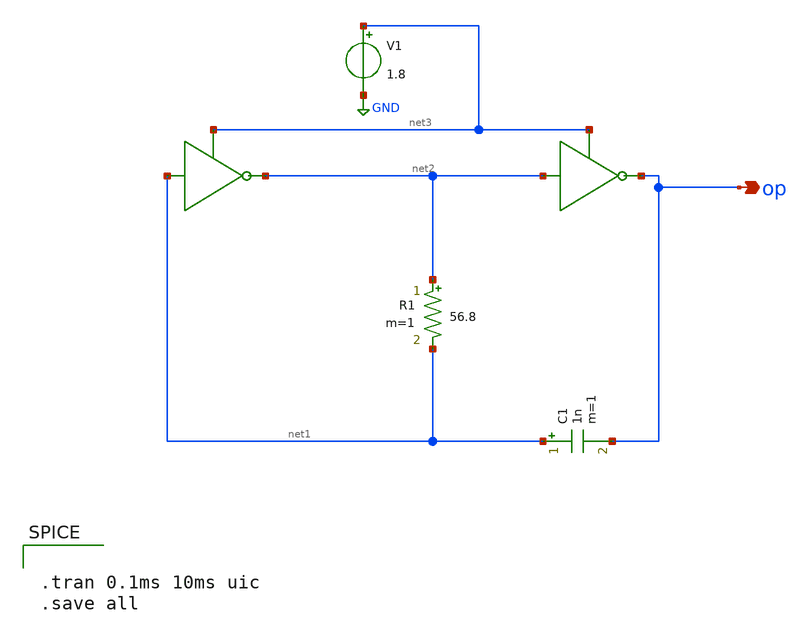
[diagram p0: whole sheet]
** sch_path: Current Sensor/sq_wave.sch
**.subckt sq_wave op
*.opin op
C1 net1 op 1n m=1
R1 net2 net1 56.8 m=1
V1 net3 GND 1.8
**** begin user architecture code


.tran 0.1ms 10ms uic
.save all


** opencircuitdesign pdks install
.lib $::SKYWATER_MODELS/sky130.lib.spice tt_mm


**** end user architecture code
**.ends
.GLOBAL GND
.end
